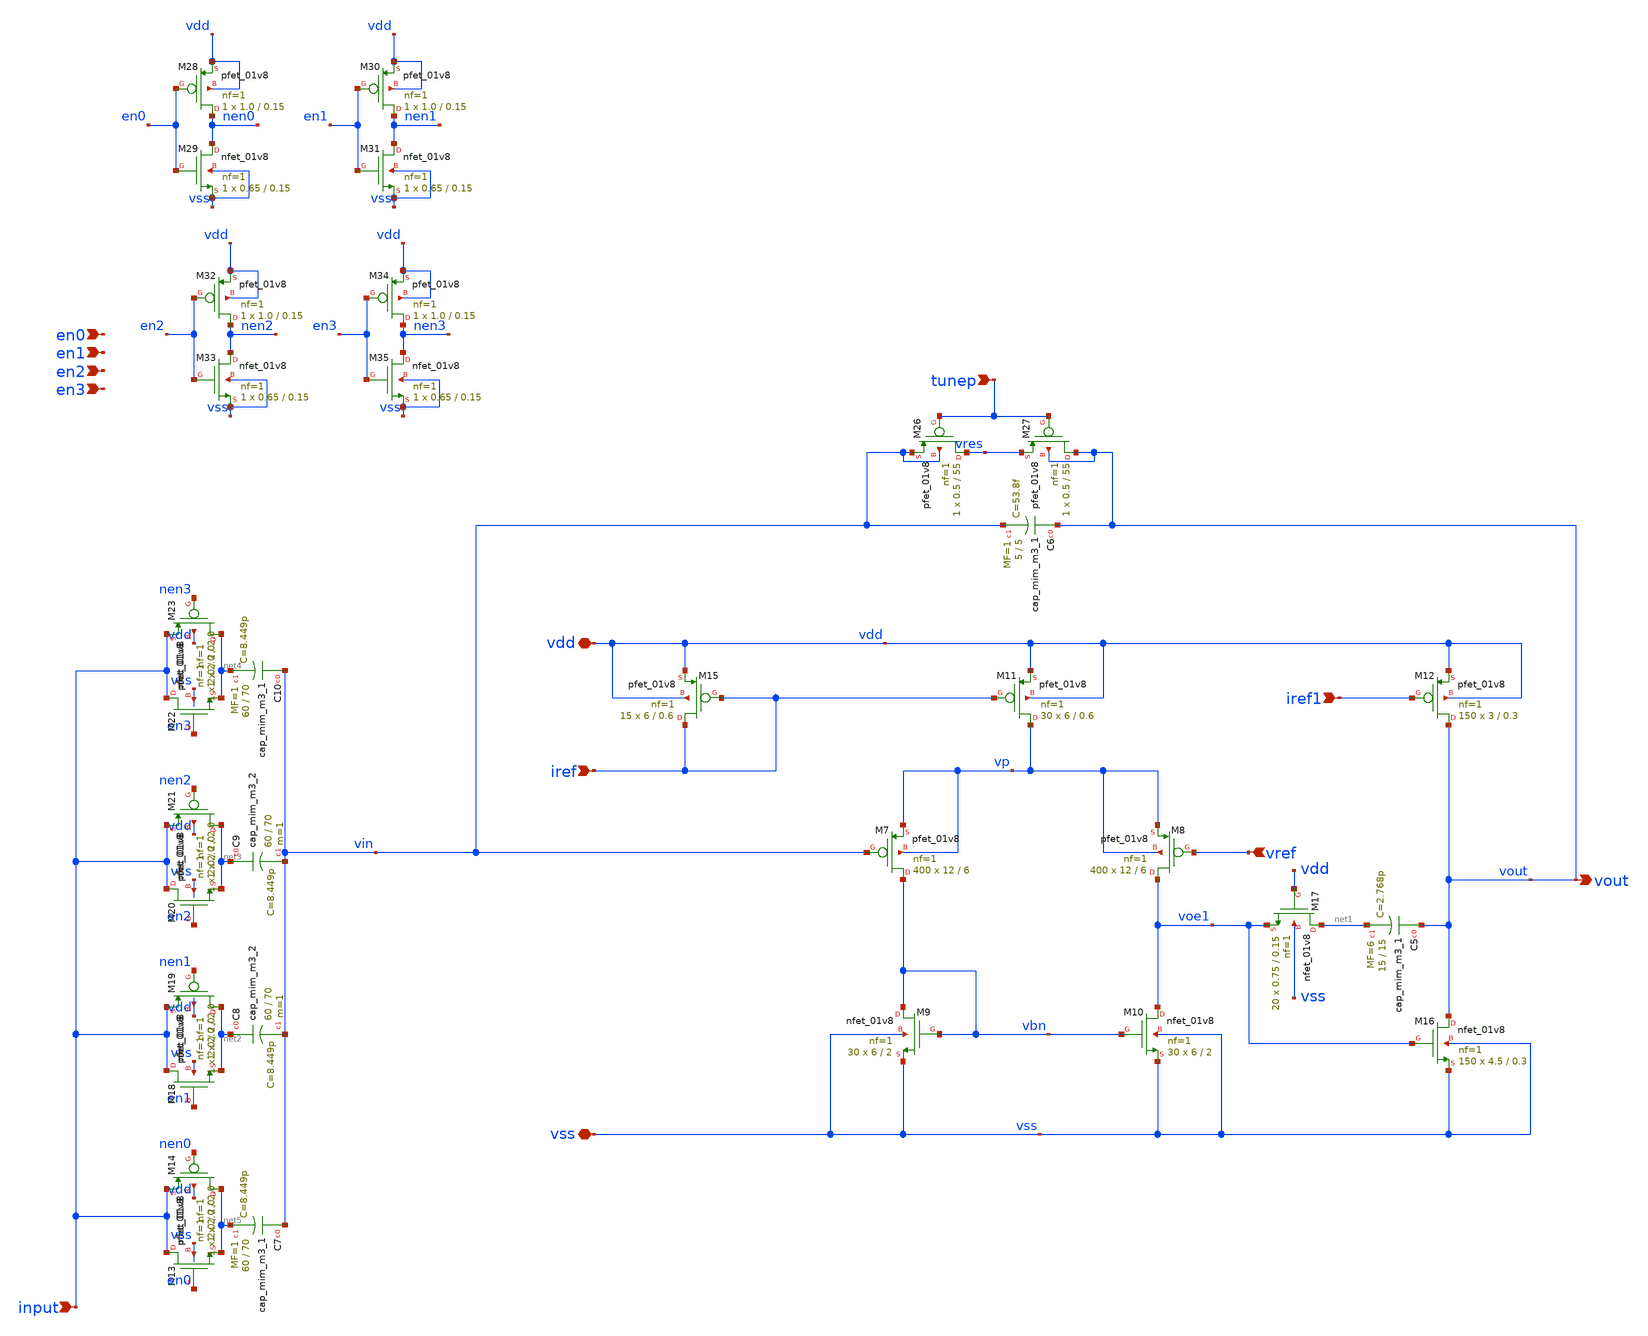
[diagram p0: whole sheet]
** sch_path: design/xschem/low_noise_amp_fc_full.sch
**.subckt low_noise_amp_fc_full vdd vss vref iref vout tunep en0 en1 en2 en3 input iref1
*.iopin vdd
*.iopin vss
*.ipin vref
*.ipin iref
*.opin vout
*.ipin tunep
*.ipin en0
*.ipin en1
*.ipin en2
*.ipin en3
*.ipin input
*.ipin iref1
XM7 vbn vin vp vp sky130_fd_pr__pfet_01v8 L=6 W=12 nf=1 ad='W * 0.29' as='W * 0.29' pd='2 * (W + 0.29)'
+ ps='2 * (W + 0.29)' nrd='0.29 / W' nrs='0.29 / W' sa=0 sb=0 sd=0 mult=400 m=400
XM8 voe1 vref vp vp sky130_fd_pr__pfet_01v8 L=6 W=12 nf=1 ad='W * 0.29' as='W * 0.29' pd='2 * (W + 0.29)'
+ ps='2 * (W + 0.29)' nrd='0.29 / W' nrs='0.29 / W' sa=0 sb=0 sd=0 mult=400 m=400
XM9 vbn vbn vss vss sky130_fd_pr__nfet_01v8 L=2 W=6 nf=1 ad='W * 0.29' as='W * 0.29' pd='2 * (W + 0.29)'
+ ps='2 * (W + 0.29)' nrd='0.29 / W' nrs='0.29 / W' sa=0 sb=0 sd=0 mult=30 m=30
XM10 voe1 vbn vss vss sky130_fd_pr__nfet_01v8 L=2 W=6 nf=1 ad='W * 0.29' as='W * 0.29' pd='2 * (W + 0.29)'
+ ps='2 * (W + 0.29)' nrd='0.29 / W' nrs='0.29 / W' sa=0 sb=0 sd=0 mult=30 m=30
XM11 vp iref vdd vdd sky130_fd_pr__pfet_01v8 L=0.6 W=6 nf=1 ad='W * 0.29' as='W * 0.29' pd='2 * (W + 0.29)'
+ ps='2 * (W + 0.29)' nrd='0.29 / W' nrs='0.29 / W' sa=0 sb=0 sd=0 mult=30 m=30
XM12 vout iref1 vdd vdd sky130_fd_pr__pfet_01v8 L=0.3 W=3 nf=1 ad='W * 0.29' as='W * 0.29' pd='2 * (W + 0.29)'
+ ps='2 * (W + 0.29)' nrd='0.29 / W' nrs='0.29 / W' sa=0 sb=0 sd=0 mult=150 m=150
XM15 iref iref vdd vdd sky130_fd_pr__pfet_01v8 L=0.6 W=6 nf=1 ad='W * 0.29' as='W * 0.29' pd='2 * (W + 0.29)'
+ ps='2 * (W + 0.29)' nrd='0.29 / W' nrs='0.29 / W' sa=0 sb=0 sd=0 mult=15 m=15
XM16 vout voe1 vss vss sky130_fd_pr__nfet_01v8 L=0.3 W=4.5 nf=1 ad='W * 0.29' as='W * 0.29' pd='2 * (W + 0.29)'
+ ps='2 * (W + 0.29)' nrd='0.29 / W' nrs='0.29 / W' sa=0 sb=0 sd=0 mult=150 m=150
XM17 net1 vdd voe1 vss sky130_fd_pr__nfet_01v8 L=0.15 W=0.75 nf=1 ad='W * 0.29' as='W * 0.29' pd='2 * (W + 0.29)'
+ ps='2 * (W + 0.29)' nrd='0.29 / W' nrs='0.29 / W' sa=0 sb=0 sd=0 mult=20 m=20
XC5 vout net1 sky130_fd_pr__cap_mim_m3_1 W=15 L=15 MF=6 m=6
XC6 vout vin sky130_fd_pr__cap_mim_m3_1 W=5 L=5 MF=1 m=1
XM26 vres tunep vin vin sky130_fd_pr__pfet_01v8 L=55 W=0.5 nf=1 ad='W * 0.29' as='W * 0.29' pd='2 * (W + 0.29)'
+ ps='2 * (W + 0.29)' nrd='0.29 / W' nrs='0.29 / W' sa=0 sb=0 sd=0 mult=1 m=1
XM27 vout tunep vres vout sky130_fd_pr__pfet_01v8 L=55 W=0.5 nf=1 ad='W * 0.29' as='W * 0.29' pd='2 * (W + 0.29)'
+ ps='2 * (W + 0.29)' nrd='0.29 / W' nrs='0.29 / W' sa=0 sb=0 sd=0 mult=1 m=1
XM28 nen0 en0 vdd vdd sky130_fd_pr__pfet_01v8 L=0.15 W=1.0 nf=1 ad='int((nf+1)/2) * W/nf * 0.29' as='int((nf+2)/2) * W/nf * 0.29'
+ pd='2*int((nf+1)/2) * (W/nf + 0.29)' ps='2*int((nf+2)/2) * (W/nf + 0.29)' nrd='0.29 / W' nrs='0.29 / W'
+ sa=0 sb=0 sd=0 mult=1 m=1
XM29 nen0 en0 vss vss sky130_fd_pr__nfet_01v8 L=0.15 W=0.65 nf=1 ad='int((nf+1)/2) * W/nf * 0.29' as='int((nf+2)/2) * W/nf * 0.29'
+ pd='2*int((nf+1)/2) * (W/nf + 0.29)' ps='2*int((nf+2)/2) * (W/nf + 0.29)' nrd='0.29 / W' nrs='0.29 / W'
+ sa=0 sb=0 sd=0 mult=1 m=1
XM30 nen1 en1 vdd vdd sky130_fd_pr__pfet_01v8 L=0.15 W=1.0 nf=1 ad='int((nf+1)/2) * W/nf * 0.29' as='int((nf+2)/2) * W/nf * 0.29'
+ pd='2*int((nf+1)/2) * (W/nf + 0.29)' ps='2*int((nf+2)/2) * (W/nf + 0.29)' nrd='0.29 / W' nrs='0.29 / W'
+ sa=0 sb=0 sd=0 mult=1 m=1
XM31 nen1 en1 vss vss sky130_fd_pr__nfet_01v8 L=0.15 W=0.65 nf=1 ad='int((nf+1)/2) * W/nf * 0.29' as='int((nf+2)/2) * W/nf * 0.29'
+ pd='2*int((nf+1)/2) * (W/nf + 0.29)' ps='2*int((nf+2)/2) * (W/nf + 0.29)' nrd='0.29 / W' nrs='0.29 / W'
+ sa=0 sb=0 sd=0 mult=1 m=1
XM32 nen2 en2 vdd vdd sky130_fd_pr__pfet_01v8 L=0.15 W=1.0 nf=1 ad='int((nf+1)/2) * W/nf * 0.29' as='int((nf+2)/2) * W/nf * 0.29'
+ pd='2*int((nf+1)/2) * (W/nf + 0.29)' ps='2*int((nf+2)/2) * (W/nf + 0.29)' nrd='0.29 / W' nrs='0.29 / W'
+ sa=0 sb=0 sd=0 mult=1 m=1
XM33 nen2 en2 vss vss sky130_fd_pr__nfet_01v8 L=0.15 W=0.65 nf=1 ad='int((nf+1)/2) * W/nf * 0.29' as='int((nf+2)/2) * W/nf * 0.29'
+ pd='2*int((nf+1)/2) * (W/nf + 0.29)' ps='2*int((nf+2)/2) * (W/nf + 0.29)' nrd='0.29 / W' nrs='0.29 / W'
+ sa=0 sb=0 sd=0 mult=1 m=1
XM34 nen3 en3 vdd vdd sky130_fd_pr__pfet_01v8 L=0.15 W=1.0 nf=1 ad='int((nf+1)/2) * W/nf * 0.29' as='int((nf+2)/2) * W/nf * 0.29'
+ pd='2*int((nf+1)/2) * (W/nf + 0.29)' ps='2*int((nf+2)/2) * (W/nf + 0.29)' nrd='0.29 / W' nrs='0.29 / W'
+ sa=0 sb=0 sd=0 mult=1 m=1
XM35 nen3 en3 vss vss sky130_fd_pr__nfet_01v8 L=0.15 W=0.65 nf=1 ad='int((nf+1)/2) * W/nf * 0.29' as='int((nf+2)/2) * W/nf * 0.29'
+ pd='2*int((nf+1)/2) * (W/nf + 0.29)' ps='2*int((nf+2)/2) * (W/nf + 0.29)' nrd='0.29 / W' nrs='0.29 / W'
+ sa=0 sb=0 sd=0 mult=1 m=1
XC7 vin net5 sky130_fd_pr__cap_mim_m3_1 W=60 L=70 MF=1 m=1
XC8 net2 vin sky130_fd_pr__cap_mim_m3_2 W=60 L=70 MF=1 m=1
XC9 net3 vin sky130_fd_pr__cap_mim_m3_2 W=60 L=70 MF=1 m=1
XC10 vin net4 sky130_fd_pr__cap_mim_m3_1 W=60 L=70 MF=1 m=1
XM13 input en0 net5 vss sky130_fd_pr__nfet_01v8 L=2.0 W=2.0 nf=1 ad='int((nf+1)/2) * W/nf * 0.29' as='int((nf+2)/2) * W/nf * 0.29'
+ pd='2*int((nf+1)/2) * (W/nf + 0.29)' ps='2*int((nf+2)/2) * (W/nf + 0.29)' nrd='0.29 / W' nrs='0.29 / W'
+ sa=0 sb=0 sd=0 mult=1 m=1
XM14 net5 nen0 input vdd sky130_fd_pr__pfet_01v8 L=2.0 W=2.0 nf=1 ad='int((nf+1)/2) * W/nf * 0.29' as='int((nf+2)/2) * W/nf * 0.29'
+ pd='2*int((nf+1)/2) * (W/nf + 0.29)' ps='2*int((nf+2)/2) * (W/nf + 0.29)' nrd='0.29 / W' nrs='0.29 / W'
+ sa=0 sb=0 sd=0 mult=1 m=1
XM18 input en1 net2 vss sky130_fd_pr__nfet_01v8 L=2.0 W=2.0 nf=1 ad='int((nf+1)/2) * W/nf * 0.29' as='int((nf+2)/2) * W/nf * 0.29'
+ pd='2*int((nf+1)/2) * (W/nf + 0.29)' ps='2*int((nf+2)/2) * (W/nf + 0.29)' nrd='0.29 / W' nrs='0.29 / W'
+ sa=0 sb=0 sd=0 mult=1 m=1
XM19 net2 nen1 input vdd sky130_fd_pr__pfet_01v8 L=2.0 W=2.0 nf=1 ad='int((nf+1)/2) * W/nf * 0.29' as='int((nf+2)/2) * W/nf * 0.29'
+ pd='2*int((nf+1)/2) * (W/nf + 0.29)' ps='2*int((nf+2)/2) * (W/nf + 0.29)' nrd='0.29 / W' nrs='0.29 / W'
+ sa=0 sb=0 sd=0 mult=1 m=1
XM20 input en2 net3 vss sky130_fd_pr__nfet_01v8 L=2.0 W=2.0 nf=1 ad='int((nf+1)/2) * W/nf * 0.29' as='int((nf+2)/2) * W/nf * 0.29'
+ pd='2*int((nf+1)/2) * (W/nf + 0.29)' ps='2*int((nf+2)/2) * (W/nf + 0.29)' nrd='0.29 / W' nrs='0.29 / W'
+ sa=0 sb=0 sd=0 mult=1 m=1
XM21 net3 nen2 input vdd sky130_fd_pr__pfet_01v8 L=2.0 W=2.0 nf=1 ad='int((nf+1)/2) * W/nf * 0.29' as='int((nf+2)/2) * W/nf * 0.29'
+ pd='2*int((nf+1)/2) * (W/nf + 0.29)' ps='2*int((nf+2)/2) * (W/nf + 0.29)' nrd='0.29 / W' nrs='0.29 / W'
+ sa=0 sb=0 sd=0 mult=1 m=1
XM22 input en3 net4 vss sky130_fd_pr__nfet_01v8 L=2.0 W=2.0 nf=1 ad='int((nf+1)/2) * W/nf * 0.29' as='int((nf+2)/2) * W/nf * 0.29'
+ pd='2*int((nf+1)/2) * (W/nf + 0.29)' ps='2*int((nf+2)/2) * (W/nf + 0.29)' nrd='0.29 / W' nrs='0.29 / W'
+ sa=0 sb=0 sd=0 mult=1 m=1
XM23 net4 nen3 input vdd sky130_fd_pr__pfet_01v8 L=2.0 W=2.0 nf=1 ad='int((nf+1)/2) * W/nf * 0.29' as='int((nf+2)/2) * W/nf * 0.29'
+ pd='2*int((nf+1)/2) * (W/nf + 0.29)' ps='2*int((nf+2)/2) * (W/nf + 0.29)' nrd='0.29 / W' nrs='0.29 / W'
+ sa=0 sb=0 sd=0 mult=1 m=1
**.ends
.end
